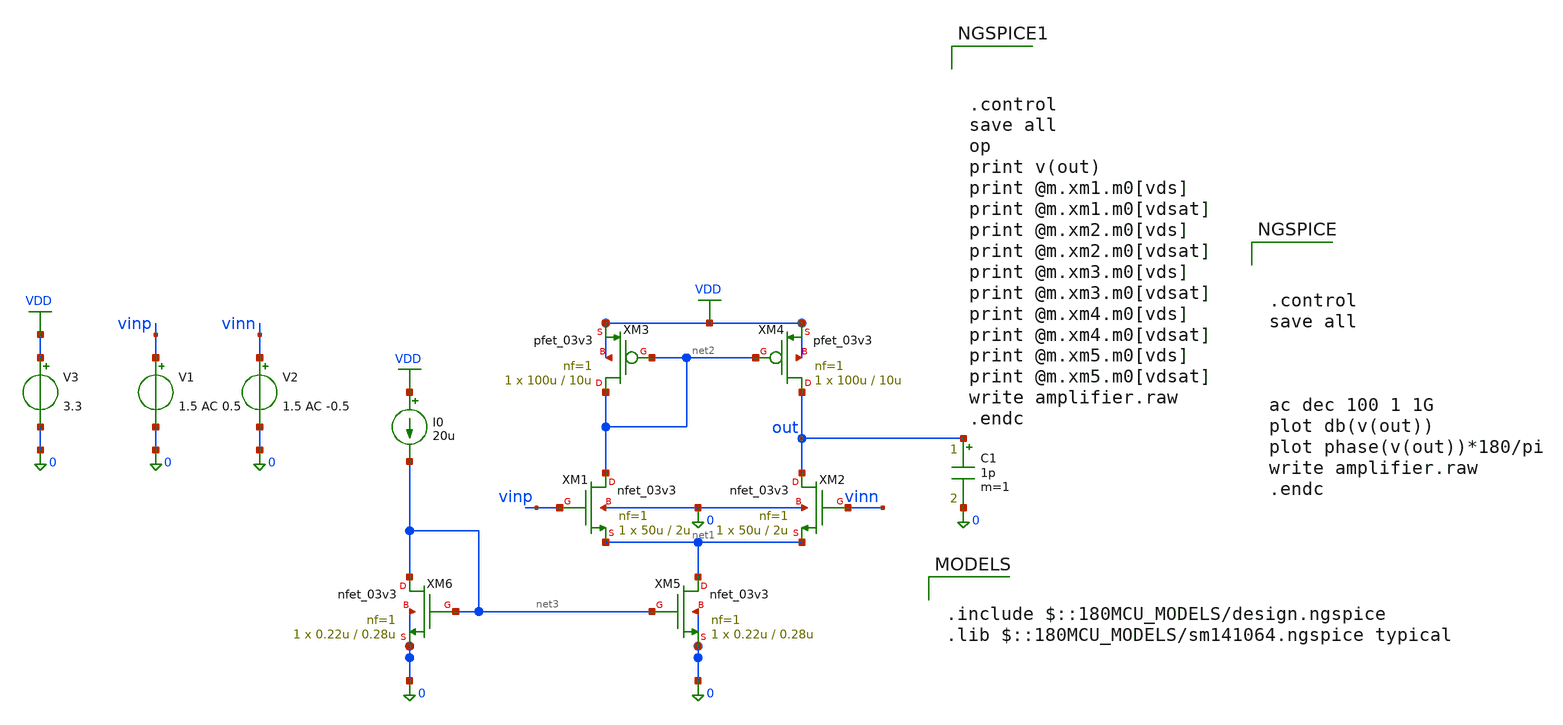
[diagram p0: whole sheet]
** sch_path: amplifier/amplifier.sch
**.subckt amplifier
XM1 net2 vinp net1 0 nfet_03v3 L=2u W=50u nf=1 ad='int((nf+1)/2) * W/nf * 0.18u' as='int((nf+2)/2) * W/nf * 0.18u'
+ pd='2*int((nf+1)/2) * (W/nf + 0.18u)' ps='2*int((nf+2)/2) * (W/nf + 0.18u)' nrd='0.18u / W' nrs='0.18u / W'
+ sa=0 sb=0 sd=0 m=1
XM2 out vinn net1 0 nfet_03v3 L=2u W=50u nf=1 ad='int((nf+1)/2) * W/nf * 0.18u' as='int((nf+2)/2) * W/nf * 0.18u'
+ pd='2*int((nf+1)/2) * (W/nf + 0.18u)' ps='2*int((nf+2)/2) * (W/nf + 0.18u)' nrd='0.18u / W' nrs='0.18u / W'
+ sa=0 sb=0 sd=0 m=1
XM3 net2 net2 VDD VDD pfet_03v3 L=10u W=100u nf=1 ad='int((nf+1)/2) * W/nf * 0.18u' as='int((nf+2)/2) * W/nf * 0.18u'
+ pd='2*int((nf+1)/2) * (W/nf + 0.18u)' ps='2*int((nf+2)/2) * (W/nf + 0.18u)' nrd='0.18u / W' nrs='0.18u / W'
+ sa=0 sb=0 sd=0 m=1
XM4 out net2 VDD VDD pfet_03v3 L=10u W=100u nf=1 ad='int((nf+1)/2) * W/nf * 0.18u' as='int((nf+2)/2) * W/nf * 0.18u'
+ pd='2*int((nf+1)/2) * (W/nf + 0.18u)' ps='2*int((nf+2)/2) * (W/nf + 0.18u)' nrd='0.18u / W' nrs='0.18u / W'
+ sa=0 sb=0 sd=0 m=1
XM5 net1 net3 0 0 nfet_03v3 L=0.28u W=0.22u nf=1 ad='int((nf+1)/2) * W/nf * 0.18u' as='int((nf+2)/2) * W/nf * 0.18u'
+ pd='2*int((nf+1)/2) * (W/nf + 0.18u)' ps='2*int((nf+2)/2) * (W/nf + 0.18u)' nrd='0.18u / W' nrs='0.18u / W'
+ sa=0 sb=0 sd=0 m=1
XM6 net3 net3 0 0 nfet_03v3 L=0.28u W=0.22u nf=1 ad='int((nf+1)/2) * W/nf * 0.18u' as='int((nf+2)/2) * W/nf * 0.18u'
+ pd='2*int((nf+1)/2) * (W/nf + 0.18u)' ps='2*int((nf+2)/2) * (W/nf + 0.18u)' nrd='0.18u / W' nrs='0.18u / W'
+ sa=0 sb=0 sd=0 m=1
V1 vinp 0 1.5 AC 0.5
V2 vinn 0 1.5 AC -0.5
V3 VDD 0 3.3
C1 out 0 1p m=1
I0 VDD net3 20u
**** begin user architecture code

.include $::180MCU_MODELS/design.ngspice
.lib $::180MCU_MODELS/sm141064.ngspice typical




.control
save all



ac dec 100 1 1G
plot db(v(out))
plot phase(v(out))*180/pi
write amplifier.raw
.endc





.control
save all
op
print v(out)
print @m.xm1.m0[vds]
print @m.xm1.m0[vdsat]
print @m.xm2.m0[vds]
print @m.xm2.m0[vdsat]
print @m.xm3.m0[vds]
print @m.xm3.m0[vdsat]
print @m.xm4.m0[vds]
print @m.xm4.m0[vdsat]
print @m.xm5.m0[vds]
print @m.xm5.m0[vdsat]
write amplifier.raw
.endc


**** end user architecture code
**.ends
.GLOBAL VDD
.end
